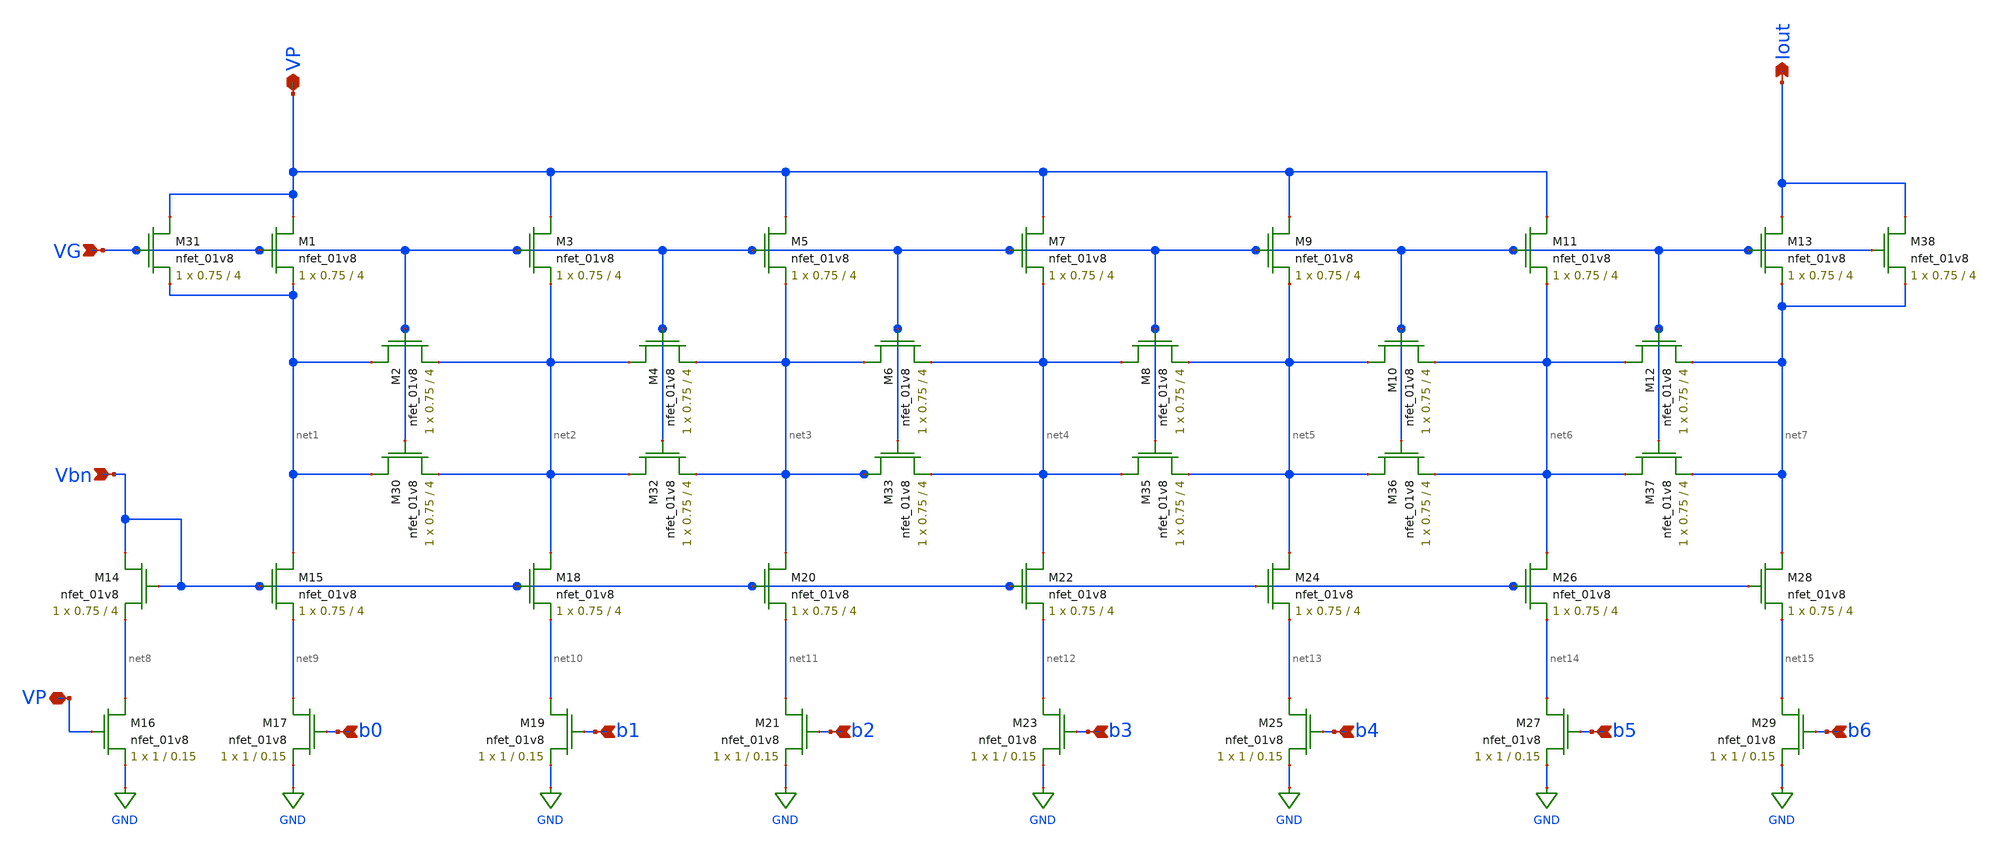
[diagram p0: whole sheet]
** sch_path: DAC.sch
**.subckt DAC VP b6 b5 b4 b3 b2 b1 b0 VP Iout VG Vbn
*.iopin VP
*.ipin b6
*.ipin b5
*.ipin b4
*.ipin b3
*.ipin b2
*.ipin b1
*.ipin b0
*.iopin VP
*.opin Iout
*.ipin VG
*.ipin Vbn
XM1 VP VG net1 GND sky130_fd_pr__nfet_01v8 L=4 W=0.75 nf=1 ad='int((nf+1)/2) * W/nf * 0.29' as='int((nf+2)/2) * W/nf * 0.29'
+ pd='2*int((nf+1)/2) * (W/nf + 0.29)' ps='2*int((nf+2)/2) * (W/nf + 0.29)' nrd='0.29 / W' nrs='0.29 / W'
+ sa=0 sb=0 sd=0 mult=1 m=1
XM2 net1 VG net2 GND sky130_fd_pr__nfet_01v8 L=4 W=0.75 nf=1 ad='int((nf+1)/2) * W/nf * 0.29' as='int((nf+2)/2) * W/nf * 0.29'
+ pd='2*int((nf+1)/2) * (W/nf + 0.29)' ps='2*int((nf+2)/2) * (W/nf + 0.29)' nrd='0.29 / W' nrs='0.29 / W'
+ sa=0 sb=0 sd=0 mult=1 m=1
XM3 VP VG net2 GND sky130_fd_pr__nfet_01v8 L=4 W=0.75 nf=1 ad='int((nf+1)/2) * W/nf * 0.29' as='int((nf+2)/2) * W/nf * 0.29'
+ pd='2*int((nf+1)/2) * (W/nf + 0.29)' ps='2*int((nf+2)/2) * (W/nf + 0.29)' nrd='0.29 / W' nrs='0.29 / W'
+ sa=0 sb=0 sd=0 mult=1 m=1
XM4 net2 VG net3 GND sky130_fd_pr__nfet_01v8 L=4 W=0.75 nf=1 ad='int((nf+1)/2) * W/nf * 0.29' as='int((nf+2)/2) * W/nf * 0.29'
+ pd='2*int((nf+1)/2) * (W/nf + 0.29)' ps='2*int((nf+2)/2) * (W/nf + 0.29)' nrd='0.29 / W' nrs='0.29 / W'
+ sa=0 sb=0 sd=0 mult=1 m=1
XM5 VP VG net3 GND sky130_fd_pr__nfet_01v8 L=4 W=0.75 nf=1 ad='int((nf+1)/2) * W/nf * 0.29' as='int((nf+2)/2) * W/nf * 0.29'
+ pd='2*int((nf+1)/2) * (W/nf + 0.29)' ps='2*int((nf+2)/2) * (W/nf + 0.29)' nrd='0.29 / W' nrs='0.29 / W'
+ sa=0 sb=0 sd=0 mult=1 m=1
XM6 net3 VG net4 GND sky130_fd_pr__nfet_01v8 L=4 W=0.75 nf=1 ad='int((nf+1)/2) * W/nf * 0.29' as='int((nf+2)/2) * W/nf * 0.29'
+ pd='2*int((nf+1)/2) * (W/nf + 0.29)' ps='2*int((nf+2)/2) * (W/nf + 0.29)' nrd='0.29 / W' nrs='0.29 / W'
+ sa=0 sb=0 sd=0 mult=1 m=1
XM7 VP VG net4 GND sky130_fd_pr__nfet_01v8 L=4 W=0.75 nf=1 ad='int((nf+1)/2) * W/nf * 0.29' as='int((nf+2)/2) * W/nf * 0.29'
+ pd='2*int((nf+1)/2) * (W/nf + 0.29)' ps='2*int((nf+2)/2) * (W/nf + 0.29)' nrd='0.29 / W' nrs='0.29 / W'
+ sa=0 sb=0 sd=0 mult=1 m=1
XM8 net4 VG net5 GND sky130_fd_pr__nfet_01v8 L=4 W=0.75 nf=1 ad='int((nf+1)/2) * W/nf * 0.29' as='int((nf+2)/2) * W/nf * 0.29'
+ pd='2*int((nf+1)/2) * (W/nf + 0.29)' ps='2*int((nf+2)/2) * (W/nf + 0.29)' nrd='0.29 / W' nrs='0.29 / W'
+ sa=0 sb=0 sd=0 mult=1 m=1
XM9 VP VG net5 GND sky130_fd_pr__nfet_01v8 L=4 W=0.75 nf=1 ad='int((nf+1)/2) * W/nf * 0.29' as='int((nf+2)/2) * W/nf * 0.29'
+ pd='2*int((nf+1)/2) * (W/nf + 0.29)' ps='2*int((nf+2)/2) * (W/nf + 0.29)' nrd='0.29 / W' nrs='0.29 / W'
+ sa=0 sb=0 sd=0 mult=1 m=1
XM10 net5 VG net6 GND sky130_fd_pr__nfet_01v8 L=4 W=0.75 nf=1 ad='int((nf+1)/2) * W/nf * 0.29' as='int((nf+2)/2) * W/nf * 0.29'
+ pd='2*int((nf+1)/2) * (W/nf + 0.29)' ps='2*int((nf+2)/2) * (W/nf + 0.29)' nrd='0.29 / W' nrs='0.29 / W'
+ sa=0 sb=0 sd=0 mult=1 m=1
XM11 VP VG net6 GND sky130_fd_pr__nfet_01v8 L=4 W=0.75 nf=1 ad='int((nf+1)/2) * W/nf * 0.29' as='int((nf+2)/2) * W/nf * 0.29'
+ pd='2*int((nf+1)/2) * (W/nf + 0.29)' ps='2*int((nf+2)/2) * (W/nf + 0.29)' nrd='0.29 / W' nrs='0.29 / W'
+ sa=0 sb=0 sd=0 mult=1 m=1
XM12 net6 VG net7 GND sky130_fd_pr__nfet_01v8 L=4 W=0.75 nf=1 ad='int((nf+1)/2) * W/nf * 0.29' as='int((nf+2)/2) * W/nf * 0.29'
+ pd='2*int((nf+1)/2) * (W/nf + 0.29)' ps='2*int((nf+2)/2) * (W/nf + 0.29)' nrd='0.29 / W' nrs='0.29 / W'
+ sa=0 sb=0 sd=0 mult=1 m=1
XM13 Iout VG net7 GND sky130_fd_pr__nfet_01v8 L=4 W=0.75 nf=1 ad='int((nf+1)/2) * W/nf * 0.29' as='int((nf+2)/2) * W/nf * 0.29'
+ pd='2*int((nf+1)/2) * (W/nf + 0.29)' ps='2*int((nf+2)/2) * (W/nf + 0.29)' nrd='0.29 / W' nrs='0.29 / W'
+ sa=0 sb=0 sd=0 mult=1 m=1
XM14 Vbn Vbn net8 GND sky130_fd_pr__nfet_01v8 L=4 W=0.75 nf=1 ad='int((nf+1)/2) * W/nf * 0.29' as='int((nf+2)/2) * W/nf * 0.29'
+ pd='2*int((nf+1)/2) * (W/nf + 0.29)' ps='2*int((nf+2)/2) * (W/nf + 0.29)' nrd='0.29 / W' nrs='0.29 / W'
+ sa=0 sb=0 sd=0 mult=1 m=1
XM15 net1 Vbn net9 GND sky130_fd_pr__nfet_01v8 L=4 W=0.75 nf=1 ad='int((nf+1)/2) * W/nf * 0.29' as='int((nf+2)/2) * W/nf * 0.29'
+ pd='2*int((nf+1)/2) * (W/nf + 0.29)' ps='2*int((nf+2)/2) * (W/nf + 0.29)' nrd='0.29 / W' nrs='0.29 / W'
+ sa=0 sb=0 sd=0 mult=1 m=1
XM16 net8 VP GND GND sky130_fd_pr__nfet_01v8 L=0.15 W=1 nf=1 ad='int((nf+1)/2) * W/nf * 0.29' as='int((nf+2)/2) * W/nf * 0.29'
+ pd='2*int((nf+1)/2) * (W/nf + 0.29)' ps='2*int((nf+2)/2) * (W/nf + 0.29)' nrd='0.29 / W' nrs='0.29 / W'
+ sa=0 sb=0 sd=0 mult=1 m=1
XM17 net9 b0 GND GND sky130_fd_pr__nfet_01v8 L=0.15 W=1 nf=1 ad='int((nf+1)/2) * W/nf * 0.29' as='int((nf+2)/2) * W/nf * 0.29'
+ pd='2*int((nf+1)/2) * (W/nf + 0.29)' ps='2*int((nf+2)/2) * (W/nf + 0.29)' nrd='0.29 / W' nrs='0.29 / W'
+ sa=0 sb=0 sd=0 mult=1 m=1
XM18 net2 Vbn net10 GND sky130_fd_pr__nfet_01v8 L=4 W=0.75 nf=1 ad='int((nf+1)/2) * W/nf * 0.29' as='int((nf+2)/2) * W/nf * 0.29'
+ pd='2*int((nf+1)/2) * (W/nf + 0.29)' ps='2*int((nf+2)/2) * (W/nf + 0.29)' nrd='0.29 / W' nrs='0.29 / W'
+ sa=0 sb=0 sd=0 mult=1 m=1
XM19 net10 b1 GND GND sky130_fd_pr__nfet_01v8 L=0.15 W=1 nf=1 ad='int((nf+1)/2) * W/nf * 0.29' as='int((nf+2)/2) * W/nf * 0.29'
+ pd='2*int((nf+1)/2) * (W/nf + 0.29)' ps='2*int((nf+2)/2) * (W/nf + 0.29)' nrd='0.29 / W' nrs='0.29 / W'
+ sa=0 sb=0 sd=0 mult=1 m=1
XM20 net3 Vbn net11 GND sky130_fd_pr__nfet_01v8 L=4 W=0.75 nf=1 ad='int((nf+1)/2) * W/nf * 0.29' as='int((nf+2)/2) * W/nf * 0.29'
+ pd='2*int((nf+1)/2) * (W/nf + 0.29)' ps='2*int((nf+2)/2) * (W/nf + 0.29)' nrd='0.29 / W' nrs='0.29 / W'
+ sa=0 sb=0 sd=0 mult=1 m=1
XM21 net11 b2 GND GND sky130_fd_pr__nfet_01v8 L=0.15 W=1 nf=1 ad='int((nf+1)/2) * W/nf * 0.29' as='int((nf+2)/2) * W/nf * 0.29'
+ pd='2*int((nf+1)/2) * (W/nf + 0.29)' ps='2*int((nf+2)/2) * (W/nf + 0.29)' nrd='0.29 / W' nrs='0.29 / W'
+ sa=0 sb=0 sd=0 mult=1 m=1
XM22 net4 Vbn net12 GND sky130_fd_pr__nfet_01v8 L=4 W=0.75 nf=1 ad='int((nf+1)/2) * W/nf * 0.29' as='int((nf+2)/2) * W/nf * 0.29'
+ pd='2*int((nf+1)/2) * (W/nf + 0.29)' ps='2*int((nf+2)/2) * (W/nf + 0.29)' nrd='0.29 / W' nrs='0.29 / W'
+ sa=0 sb=0 sd=0 mult=1 m=1
XM23 net12 b3 GND GND sky130_fd_pr__nfet_01v8 L=0.15 W=1 nf=1 ad='int((nf+1)/2) * W/nf * 0.29' as='int((nf+2)/2) * W/nf * 0.29'
+ pd='2*int((nf+1)/2) * (W/nf + 0.29)' ps='2*int((nf+2)/2) * (W/nf + 0.29)' nrd='0.29 / W' nrs='0.29 / W'
+ sa=0 sb=0 sd=0 mult=1 m=1
XM24 net5 Vbn net13 GND sky130_fd_pr__nfet_01v8 L=4 W=0.75 nf=1 ad='int((nf+1)/2) * W/nf * 0.29' as='int((nf+2)/2) * W/nf * 0.29'
+ pd='2*int((nf+1)/2) * (W/nf + 0.29)' ps='2*int((nf+2)/2) * (W/nf + 0.29)' nrd='0.29 / W' nrs='0.29 / W'
+ sa=0 sb=0 sd=0 mult=1 m=1
XM25 net13 b4 GND GND sky130_fd_pr__nfet_01v8 L=0.15 W=1 nf=1 ad='int((nf+1)/2) * W/nf * 0.29' as='int((nf+2)/2) * W/nf * 0.29'
+ pd='2*int((nf+1)/2) * (W/nf + 0.29)' ps='2*int((nf+2)/2) * (W/nf + 0.29)' nrd='0.29 / W' nrs='0.29 / W'
+ sa=0 sb=0 sd=0 mult=1 m=1
XM26 net6 Vbn net14 GND sky130_fd_pr__nfet_01v8 L=4 W=0.75 nf=1 ad='int((nf+1)/2) * W/nf * 0.29' as='int((nf+2)/2) * W/nf * 0.29'
+ pd='2*int((nf+1)/2) * (W/nf + 0.29)' ps='2*int((nf+2)/2) * (W/nf + 0.29)' nrd='0.29 / W' nrs='0.29 / W'
+ sa=0 sb=0 sd=0 mult=1 m=1
XM27 net14 b5 GND GND sky130_fd_pr__nfet_01v8 L=0.15 W=1 nf=1 ad='int((nf+1)/2) * W/nf * 0.29' as='int((nf+2)/2) * W/nf * 0.29'
+ pd='2*int((nf+1)/2) * (W/nf + 0.29)' ps='2*int((nf+2)/2) * (W/nf + 0.29)' nrd='0.29 / W' nrs='0.29 / W'
+ sa=0 sb=0 sd=0 mult=1 m=1
XM28 net7 Vbn net15 GND sky130_fd_pr__nfet_01v8 L=4 W=0.75 nf=1 ad='int((nf+1)/2) * W/nf * 0.29' as='int((nf+2)/2) * W/nf * 0.29'
+ pd='2*int((nf+1)/2) * (W/nf + 0.29)' ps='2*int((nf+2)/2) * (W/nf + 0.29)' nrd='0.29 / W' nrs='0.29 / W'
+ sa=0 sb=0 sd=0 mult=1 m=1
XM29 net15 b6 GND GND sky130_fd_pr__nfet_01v8 L=0.15 W=1 nf=1 ad='int((nf+1)/2) * W/nf * 0.29' as='int((nf+2)/2) * W/nf * 0.29'
+ pd='2*int((nf+1)/2) * (W/nf + 0.29)' ps='2*int((nf+2)/2) * (W/nf + 0.29)' nrd='0.29 / W' nrs='0.29 / W'
+ sa=0 sb=0 sd=0 mult=1 m=1
XM30 net1 VG net2 GND sky130_fd_pr__nfet_01v8 L=4 W=0.75 nf=1 ad='int((nf+1)/2) * W/nf * 0.29' as='int((nf+2)/2) * W/nf * 0.29'
+ pd='2*int((nf+1)/2) * (W/nf + 0.29)' ps='2*int((nf+2)/2) * (W/nf + 0.29)' nrd='0.29 / W' nrs='0.29 / W'
+ sa=0 sb=0 sd=0 mult=1 m=1
XM31 VP VG net1 GND sky130_fd_pr__nfet_01v8 L=4 W=0.75 nf=1 ad='int((nf+1)/2) * W/nf * 0.29' as='int((nf+2)/2) * W/nf * 0.29'
+ pd='2*int((nf+1)/2) * (W/nf + 0.29)' ps='2*int((nf+2)/2) * (W/nf + 0.29)' nrd='0.29 / W' nrs='0.29 / W'
+ sa=0 sb=0 sd=0 mult=1 m=1
XM32 net2 VG net3 GND sky130_fd_pr__nfet_01v8 L=4 W=0.75 nf=1 ad='int((nf+1)/2) * W/nf * 0.29' as='int((nf+2)/2) * W/nf * 0.29'
+ pd='2*int((nf+1)/2) * (W/nf + 0.29)' ps='2*int((nf+2)/2) * (W/nf + 0.29)' nrd='0.29 / W' nrs='0.29 / W'
+ sa=0 sb=0 sd=0 mult=1 m=1
XM33 net3 VG net4 GND sky130_fd_pr__nfet_01v8 L=4 W=0.75 nf=1 ad='int((nf+1)/2) * W/nf * 0.29' as='int((nf+2)/2) * W/nf * 0.29'
+ pd='2*int((nf+1)/2) * (W/nf + 0.29)' ps='2*int((nf+2)/2) * (W/nf + 0.29)' nrd='0.29 / W' nrs='0.29 / W'
+ sa=0 sb=0 sd=0 mult=1 m=1
XM35 net4 VG net5 GND sky130_fd_pr__nfet_01v8 L=4 W=0.75 nf=1 ad='int((nf+1)/2) * W/nf * 0.29' as='int((nf+2)/2) * W/nf * 0.29'
+ pd='2*int((nf+1)/2) * (W/nf + 0.29)' ps='2*int((nf+2)/2) * (W/nf + 0.29)' nrd='0.29 / W' nrs='0.29 / W'
+ sa=0 sb=0 sd=0 mult=1 m=1
XM36 net5 VG net6 GND sky130_fd_pr__nfet_01v8 L=4 W=0.75 nf=1 ad='int((nf+1)/2) * W/nf * 0.29' as='int((nf+2)/2) * W/nf * 0.29'
+ pd='2*int((nf+1)/2) * (W/nf + 0.29)' ps='2*int((nf+2)/2) * (W/nf + 0.29)' nrd='0.29 / W' nrs='0.29 / W'
+ sa=0 sb=0 sd=0 mult=1 m=1
XM37 net6 VG net7 GND sky130_fd_pr__nfet_01v8 L=4 W=0.75 nf=1 ad='int((nf+1)/2) * W/nf * 0.29' as='int((nf+2)/2) * W/nf * 0.29'
+ pd='2*int((nf+1)/2) * (W/nf + 0.29)' ps='2*int((nf+2)/2) * (W/nf + 0.29)' nrd='0.29 / W' nrs='0.29 / W'
+ sa=0 sb=0 sd=0 mult=1 m=1
XM38 Iout VG net7 GND sky130_fd_pr__nfet_01v8 L=4 W=0.75 nf=1 ad='int((nf+1)/2) * W/nf * 0.29' as='int((nf+2)/2) * W/nf * 0.29'
+ pd='2*int((nf+1)/2) * (W/nf + 0.29)' ps='2*int((nf+2)/2) * (W/nf + 0.29)' nrd='0.29 / W' nrs='0.29 / W'
+ sa=0 sb=0 sd=0 mult=1 m=1
**.ends
.GLOBAL GND
.end
